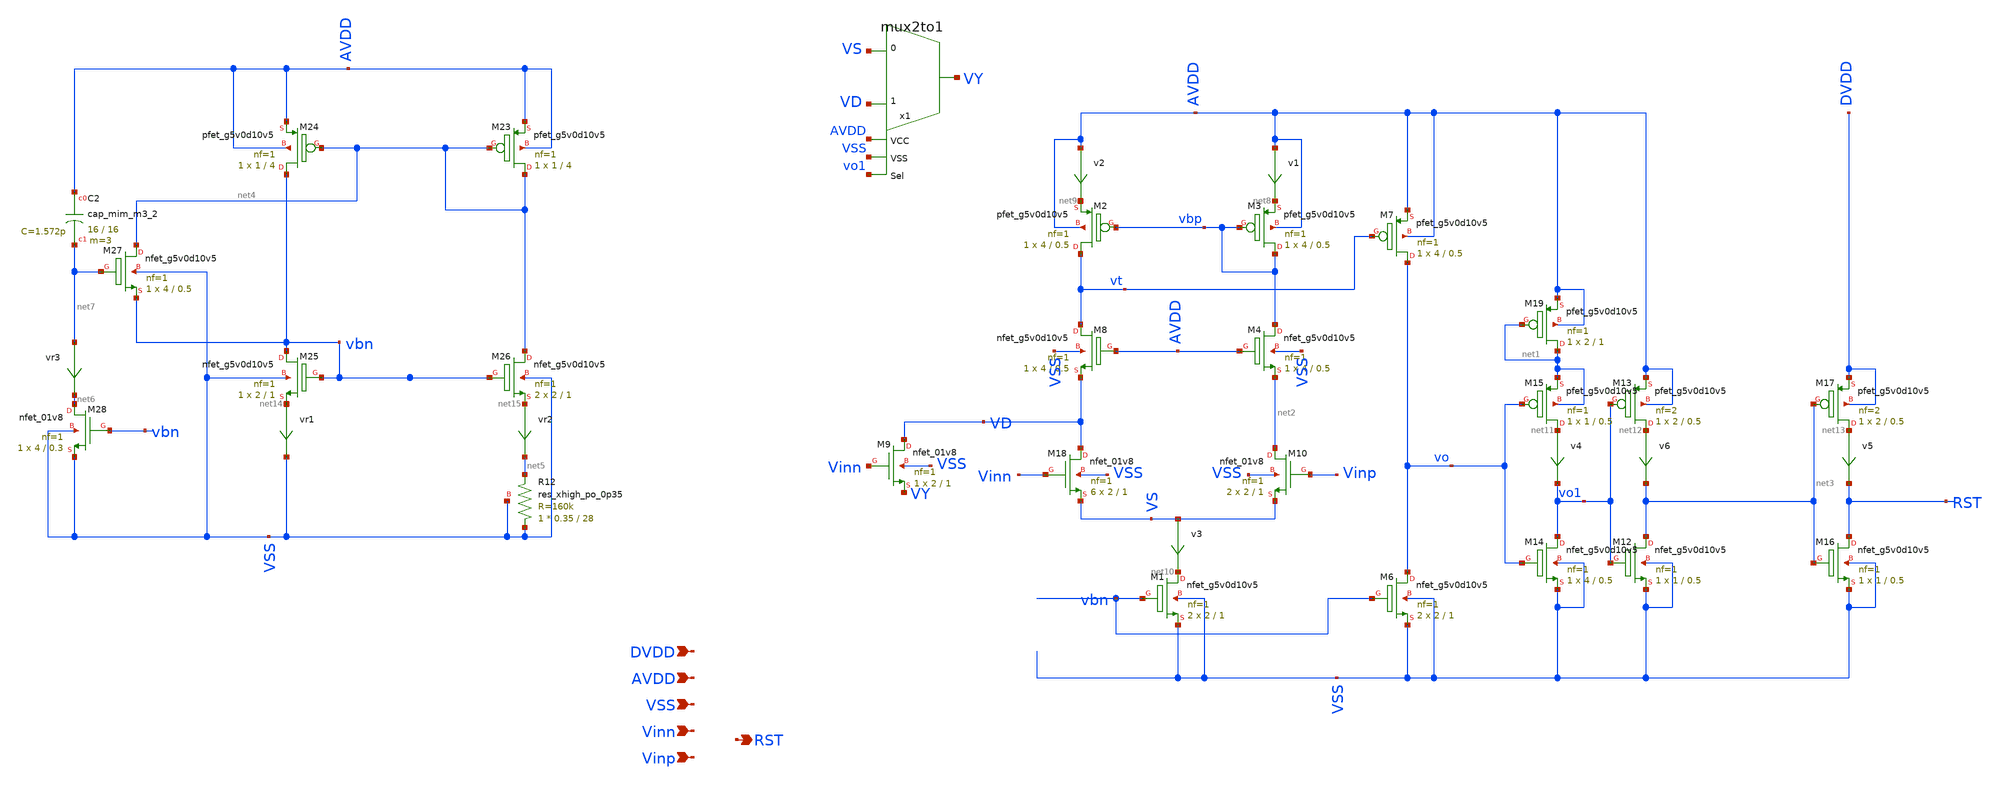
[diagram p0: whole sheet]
** sch_path: xschem/comparator_final.sch
**.subckt comparator_final AVDD RST VSS Vinn Vinp DVDD
*.ipin AVDD
*.opin RST
*.ipin VSS
*.ipin Vinn
*.ipin Vinp
*.ipin DVDD
v1 AVDD net8 0
.save i(v1)
v2 AVDD net9 0
.save i(v2)
XM1 net10 vbn VSS VSS sky130_fd_pr__nfet_g5v0d10v5 L=1 W=2 nf=1 ad='int((nf+1)/2) * W/nf * 0.29' as='int((nf+2)/2) * W/nf * 0.29'
+ pd='2*int((nf+1)/2) * (W/nf + 0.29)' ps='2*int((nf+2)/2) * (W/nf + 0.29)' nrd='0.29 / W' nrs='0.29 / W'
+ sa=0 sb=0 sd=0 mult=2 m=2
XM3 vbp vbp net8 AVDD sky130_fd_pr__pfet_g5v0d10v5 L=0.5 W=4 nf=1 ad='int((nf+1)/2) * W/nf * 0.29' as='int((nf+2)/2) * W/nf * 0.29'
+ pd='2*int((nf+1)/2) * (W/nf + 0.29)' ps='2*int((nf+2)/2) * (W/nf + 0.29)' nrd='0.29 / W' nrs='0.29 / W'
+ sa=0 sb=0 sd=0 mult=1 m=1
XM2 vt vbp net9 AVDD sky130_fd_pr__pfet_g5v0d10v5 L=0.5 W=4 nf=1 ad='int((nf+1)/2) * W/nf * 0.29' as='int((nf+2)/2) * W/nf * 0.29'
+ pd='2*int((nf+1)/2) * (W/nf + 0.29)' ps='2*int((nf+2)/2) * (W/nf + 0.29)' nrd='0.29 / W' nrs='0.29 / W'
+ sa=0 sb=0 sd=0 mult=1 m=1
v4 net11 vo1 0
.save i(v4)
XM7 vo vt AVDD AVDD sky130_fd_pr__pfet_g5v0d10v5 L=0.5 W=4 nf=1 ad='int((nf+1)/2) * W/nf * 0.29' as='int((nf+2)/2) * W/nf * 0.29'
+ pd='2*int((nf+1)/2) * (W/nf + 0.29)' ps='2*int((nf+2)/2) * (W/nf + 0.29)' nrd='0.29 / W' nrs='0.29 / W'
+ sa=0 sb=0 sd=0 mult=1 m=1
v3 VS net10 0
.save i(v3)
x1 VD VS VY AVDD VSS vo1 mux2to1
XM6 vo vbn VSS VSS sky130_fd_pr__nfet_g5v0d10v5 L=1 W=2 nf=1 ad='int((nf+1)/2) * W/nf * 0.29' as='int((nf+2)/2) * W/nf * 0.29'
+ pd='2*int((nf+1)/2) * (W/nf + 0.29)' ps='2*int((nf+2)/2) * (W/nf + 0.29)' nrd='0.29 / W' nrs='0.29 / W'
+ sa=0 sb=0 sd=0 mult=2 m=2
v6 net12 net3 0
.save i(v6)
XM14 vo1 vo VSS VSS sky130_fd_pr__nfet_g5v0d10v5 L=0.5 W=4 nf=1 ad='int((nf+1)/2) * W/nf * 0.29' as='int((nf+2)/2) * W/nf * 0.29'
+ pd='2*int((nf+1)/2) * (W/nf + 0.29)' ps='2*int((nf+2)/2) * (W/nf + 0.29)' nrd='0.29 / W' nrs='0.29 / W'
+ sa=0 sb=0 sd=0 mult=1 m=1
XM15 net11 vo net1 net1 sky130_fd_pr__pfet_g5v0d10v5 L=0.5 W=1 nf=1 ad='int((nf+1)/2) * W/nf * 0.29'
+ as='int((nf+2)/2) * W/nf * 0.29' pd='2*int((nf+1)/2) * (W/nf + 0.29)' ps='2*int((nf+2)/2) * (W/nf + 0.29)'
+ nrd='0.29 / W' nrs='0.29 / W' sa=0 sb=0 sd=0 mult=1 m=1
XM12 net3 vo1 VSS VSS sky130_fd_pr__nfet_g5v0d10v5 L=0.5 W=1 nf=1 ad='int((nf+1)/2) * W/nf * 0.29' as='int((nf+2)/2) * W/nf * 0.29'
+ pd='2*int((nf+1)/2) * (W/nf + 0.29)' ps='2*int((nf+2)/2) * (W/nf + 0.29)' nrd='0.29 / W' nrs='0.29 / W'
+ sa=0 sb=0 sd=0 mult=1 m=1
XM13 net12 vo1 AVDD AVDD sky130_fd_pr__pfet_g5v0d10v5 L=0.5 W=2 nf=2 ad='int((nf+1)/2) * W/nf * 0.29'
+ as='int((nf+2)/2) * W/nf * 0.29' pd='2*int((nf+1)/2) * (W/nf + 0.29)' ps='2*int((nf+2)/2) * (W/nf + 0.29)'
+ nrd='0.29 / W' nrs='0.29 / W' sa=0 sb=0 sd=0 mult=1 m=1
v5 net13 RST 0
.save i(v5)
XM16 RST net3 VSS VSS sky130_fd_pr__nfet_g5v0d10v5 L=0.5 W=1 nf=1 ad='int((nf+1)/2) * W/nf * 0.29' as='int((nf+2)/2) * W/nf * 0.29'
+ pd='2*int((nf+1)/2) * (W/nf + 0.29)' ps='2*int((nf+2)/2) * (W/nf + 0.29)' nrd='0.29 / W' nrs='0.29 / W'
+ sa=0 sb=0 sd=0 mult=1 m=1
XM17 net13 net3 DVDD DVDD sky130_fd_pr__pfet_g5v0d10v5 L=0.5 W=2 nf=2 ad='int((nf+1)/2) * W/nf * 0.29'
+ as='int((nf+2)/2) * W/nf * 0.29' pd='2*int((nf+1)/2) * (W/nf + 0.29)' ps='2*int((nf+2)/2) * (W/nf + 0.29)'
+ nrd='0.29 / W' nrs='0.29 / W' sa=0 sb=0 sd=0 mult=1 m=1
XM4 vbp AVDD net2 VSS sky130_fd_pr__nfet_g5v0d10v5 L=0.5 W=4 nf=1 ad='int((nf+1)/2) * W/nf * 0.29' as='int((nf+2)/2) * W/nf * 0.29'
+ pd='2*int((nf+1)/2) * (W/nf + 0.29)' ps='2*int((nf+2)/2) * (W/nf + 0.29)' nrd='0.29 / W' nrs='0.29 / W'
+ sa=0 sb=0 sd=0 mult=1 m=1
XM8 vt AVDD VD VSS sky130_fd_pr__nfet_g5v0d10v5 L=0.5 W=4 nf=1 ad='int((nf+1)/2) * W/nf * 0.29' as='int((nf+2)/2) * W/nf * 0.29'
+ pd='2*int((nf+1)/2) * (W/nf + 0.29)' ps='2*int((nf+2)/2) * (W/nf + 0.29)' nrd='0.29 / W' nrs='0.29 / W'
+ sa=0 sb=0 sd=0 mult=1 m=1
XM19 net1 net1 AVDD AVDD sky130_fd_pr__pfet_g5v0d10v5 L=1 W=2 nf=1 ad='int((nf+1)/2) * W/nf * 0.29' as='int((nf+2)/2) * W/nf * 0.29'
+ pd='2*int((nf+1)/2) * (W/nf + 0.29)' ps='2*int((nf+2)/2) * (W/nf + 0.29)' nrd='0.29 / W' nrs='0.29 / W'
+ sa=0 sb=0 sd=0 mult=1 m=1
XM23 net4 net4 AVDD AVDD sky130_fd_pr__pfet_g5v0d10v5 L=4 W=1 nf=1 ad='int((nf+1)/2) * W/nf * 0.29' as='int((nf+2)/2) * W/nf * 0.29'
+ pd='2*int((nf+1)/2) * (W/nf + 0.29)' ps='2*int((nf+2)/2) * (W/nf + 0.29)' nrd='0.29 / W' nrs='0.29 / W'
+ sa=0 sb=0 sd=0 mult=1 m=1
XM24 vbn net4 AVDD AVDD sky130_fd_pr__pfet_g5v0d10v5 L=4 W=1 nf=1 ad='int((nf+1)/2) * W/nf * 0.29' as='int((nf+2)/2) * W/nf * 0.29'
+ pd='2*int((nf+1)/2) * (W/nf + 0.29)' ps='2*int((nf+2)/2) * (W/nf + 0.29)' nrd='0.29 / W' nrs='0.29 / W'
+ sa=0 sb=0 sd=0 mult=1 m=1
XR12 VSS net5 VSS sky130_fd_pr__res_xhigh_po_0p35 L=28 mult=1 m=1
vr1 net14 VSS 0
.save i(vr1)
vr2 net15 net5 0
.save i(vr2)
vr3 net7 net6 0
.save i(vr3)
XM25 vbn vbn net14 VSS sky130_fd_pr__nfet_g5v0d10v5 L=1 W=2 nf=1 ad='int((nf+1)/2) * W/nf * 0.29' as='int((nf+2)/2) * W/nf * 0.29'
+ pd='2*int((nf+1)/2) * (W/nf + 0.29)' ps='2*int((nf+2)/2) * (W/nf + 0.29)' nrd='0.29 / W' nrs='0.29 / W'
+ sa=0 sb=0 sd=0 mult=1 m=1
XM26 net4 vbn net15 VSS sky130_fd_pr__nfet_g5v0d10v5 L=1 W=2 nf=1 ad='int((nf+1)/2) * W/nf * 0.29' as='int((nf+2)/2) * W/nf * 0.29'
+ pd='2*int((nf+1)/2) * (W/nf + 0.29)' ps='2*int((nf+2)/2) * (W/nf + 0.29)' nrd='0.29 / W' nrs='0.29 / W'
+ sa=0 sb=0 sd=0 mult=2 m=2
XM27 net4 net7 vbn VSS sky130_fd_pr__nfet_g5v0d10v5 L=0.5 W=4 nf=1 ad='int((nf+1)/2) * W/nf * 0.29' as='int((nf+2)/2) * W/nf * 0.29'
+ pd='2*int((nf+1)/2) * (W/nf + 0.29)' ps='2*int((nf+2)/2) * (W/nf + 0.29)' nrd='0.29 / W' nrs='0.29 / W'
+ sa=0 sb=0 sd=0 mult=1 m=1
XM28 net6 vbn VSS VSS sky130_fd_pr__nfet_01v8 L=0.3 W=4 nf=1 ad='int((nf+1)/2) * W/nf * 0.29' as='int((nf+2)/2) * W/nf * 0.29'
+ pd='2*int((nf+1)/2) * (W/nf + 0.29)' ps='2*int((nf+2)/2) * (W/nf + 0.29)' nrd='0.29 / W' nrs='0.29 / W'
+ sa=0 sb=0 sd=0 mult=1 m=1
XM18 VD Vinn VS VSS sky130_fd_pr__nfet_01v8 L=1 W=2 nf=1 ad='int((nf+1)/2) * W/nf * 0.29' as='int((nf+2)/2) * W/nf * 0.29'
+ pd='2*int((nf+1)/2) * (W/nf + 0.29)' ps='2*int((nf+2)/2) * (W/nf + 0.29)' nrd='0.29 / W' nrs='0.29 / W'
+ sa=0 sb=0 sd=0 mult=6 m=6
XM9 VD Vinn VY VSS sky130_fd_pr__nfet_01v8 L=1 W=2 nf=1 ad='int((nf+1)/2) * W/nf * 0.29' as='int((nf+2)/2) * W/nf * 0.29'
+ pd='2*int((nf+1)/2) * (W/nf + 0.29)' ps='2*int((nf+2)/2) * (W/nf + 0.29)' nrd='0.29 / W' nrs='0.29 / W'
+ sa=0 sb=0 sd=0 mult=1 m=1
XM10 net2 Vinp VS VSS sky130_fd_pr__nfet_01v8 L=1 W=2 nf=1 ad='int((nf+1)/2) * W/nf * 0.29' as='int((nf+2)/2) * W/nf * 0.29'
+ pd='2*int((nf+1)/2) * (W/nf + 0.29)' ps='2*int((nf+2)/2) * (W/nf + 0.29)' nrd='0.29 / W' nrs='0.29 / W'
+ sa=0 sb=0 sd=0 mult=2 m=2
XC2 AVDD net7 sky130_fd_pr__cap_mim_m3_2 W=16 L=16 MF=3 m=3
**.ends
.end
